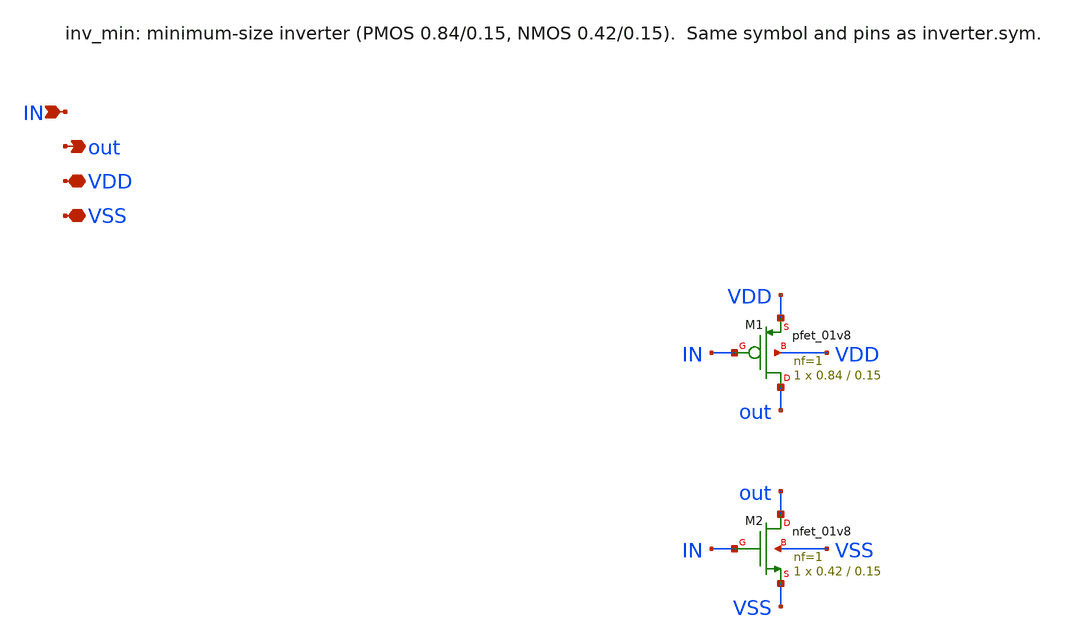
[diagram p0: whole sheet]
** sch_path: SAR_improved/inv_min.sch
**.subckt inv_min IN out VDD VSS
*.ipin IN
*.opin out
*.iopin VDD
*.iopin VSS
XM1 out IN VDD VDD sky130_fd_pr__pfet_01v8 L=0.15 W=0.84 nf=1 ad='int((nf+1)/2) * W/nf * 0.29' as='int((nf+2)/2) * W/nf * 0.29'
+ pd='2*int((nf+1)/2) * (W/nf + 0.29)' ps='2*int((nf+2)/2) * (W/nf + 0.29)' nrd='0.29 / W' nrs='0.29 / W'
+ sa=0 sb=0 sd=0 mult=1 m=1
XM2 out IN VSS VSS sky130_fd_pr__nfet_01v8 L=0.15 W=0.42 nf=1 ad='int((nf+1)/2) * W/nf * 0.29' as='int((nf+2)/2) * W/nf * 0.29'
+ pd='2*int((nf+1)/2) * (W/nf + 0.29)' ps='2*int((nf+2)/2) * (W/nf + 0.29)' nrd='0.29 / W' nrs='0.29 / W'
+ sa=0 sb=0 sd=0 mult=1 m=1
**.ends
.end
